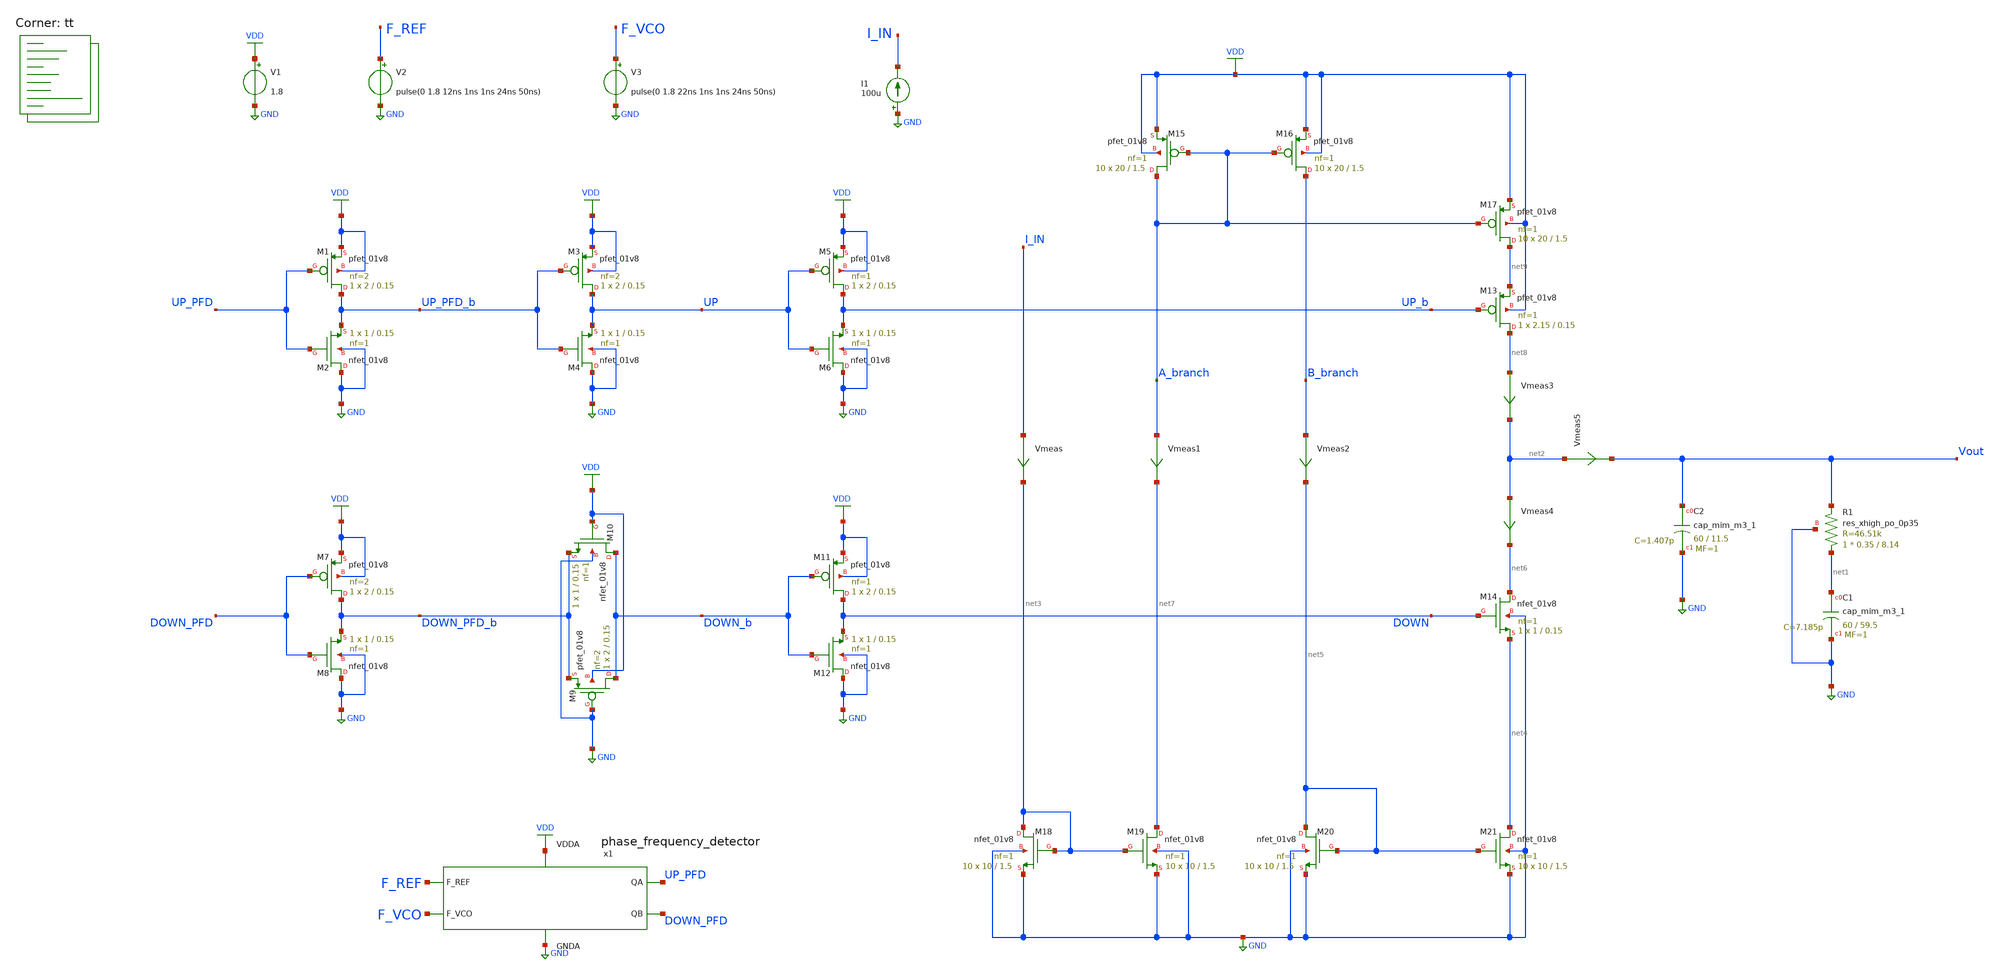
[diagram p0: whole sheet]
** sch_path: projects/pll/charge_pump/xschem_ngspice/pfd_charge_pump_dead_zone_check_2.sch
**.subckt pfd_charge_pump_dead_zone_check_2
V1 VDD GND 1.8
XC2 Vout GND sky130_fd_pr__cap_mim_m3_1 W=60 L=11.5 MF=1 m=1
XC1 net1 GND sky130_fd_pr__cap_mim_m3_1 W=60 L=59.5 MF=1 m=1
V2 F_REF GND pulse(0 1.8 12ns 1ns 1ns 24ns 50ns)
V3 F_VCO GND pulse(0 1.8 22ns 1ns 1ns 24ns 50ns)
x1 F_REF F_VCO VDD UP_PFD DOWN_PFD GND phase_frequency_detector
XR1 net1 Vout GND sky130_fd_pr__res_xhigh_po_0p35 L=8.14 mult=1 m=1
I1 GND I_IN 100u
Vmeas5 net2 Vout 0
.save i(vmeas5)
XM18 net3 net3 GND GND sky130_fd_pr__nfet_01v8 L=1.5 W=10 nf=1 ad='int((nf+1)/2) * W/nf * 0.29' as='int((nf+2)/2) * W/nf * 0.29'
+ pd='2*int((nf+1)/2) * (W/nf + 0.29)' ps='2*int((nf+2)/2) * (W/nf + 0.29)' nrd='0.29 / W' nrs='0.29 / W'
+ sa=0 sb=0 sd=0 mult=10 m=10
XM19 net7 net3 GND GND sky130_fd_pr__nfet_01v8 L=1.5 W=10 nf=1 ad='int((nf+1)/2) * W/nf * 0.29' as='int((nf+2)/2) * W/nf * 0.29'
+ pd='2*int((nf+1)/2) * (W/nf + 0.29)' ps='2*int((nf+2)/2) * (W/nf + 0.29)' nrd='0.29 / W' nrs='0.29 / W'
+ sa=0 sb=0 sd=0 mult=10 m=10
Vmeas I_IN net3 0
.save i(vmeas)
XM13 net8 UP_b net9 VDD sky130_fd_pr__pfet_01v8 L=0.15 W=2.15 nf=1 ad='int((nf+1)/2) * W/nf * 0.29' as='int((nf+2)/2) * W/nf * 0.29'
+ pd='2*int((nf+1)/2) * (W/nf + 0.29)' ps='2*int((nf+2)/2) * (W/nf + 0.29)' nrd='0.29 / W' nrs='0.29 / W'
+ sa=0 sb=0 sd=0 mult=1 m=1
Vmeas3 net8 net2 0
.save i(vmeas3)
Vmeas4 net2 net6 0
.save i(vmeas4)
XM14 net6 DOWN net4 GND sky130_fd_pr__nfet_01v8 L=0.15 W=1 nf=1 ad='int((nf+1)/2) * W/nf * 0.29' as='int((nf+2)/2) * W/nf * 0.29'
+ pd='2*int((nf+1)/2) * (W/nf + 0.29)' ps='2*int((nf+2)/2) * (W/nf + 0.29)' nrd='0.29 / W' nrs='0.29 / W'
+ sa=0 sb=0 sd=0 mult=1 m=1
XM17 net9 A_branch VDD VDD sky130_fd_pr__pfet_01v8 L=1.5 W=20 nf=1 ad='int((nf+1)/2) * W/nf * 0.29' as='int((nf+2)/2) * W/nf * 0.29'
+ pd='2*int((nf+1)/2) * (W/nf + 0.29)' ps='2*int((nf+2)/2) * (W/nf + 0.29)' nrd='0.29 / W' nrs='0.29 / W'
+ sa=0 sb=0 sd=0 mult=10 m=10
XM21 net4 net5 GND GND sky130_fd_pr__nfet_01v8 L=1.5 W=10 nf=1 ad='int((nf+1)/2) * W/nf * 0.29' as='int((nf+2)/2) * W/nf * 0.29'
+ pd='2*int((nf+1)/2) * (W/nf + 0.29)' ps='2*int((nf+2)/2) * (W/nf + 0.29)' nrd='0.29 / W' nrs='0.29 / W'
+ sa=0 sb=0 sd=0 mult=10 m=10
XM20 net5 net5 GND GND sky130_fd_pr__nfet_01v8 L=1.5 W=10 nf=1 ad='int((nf+1)/2) * W/nf * 0.29' as='int((nf+2)/2) * W/nf * 0.29'
+ pd='2*int((nf+1)/2) * (W/nf + 0.29)' ps='2*int((nf+2)/2) * (W/nf + 0.29)' nrd='0.29 / W' nrs='0.29 / W'
+ sa=0 sb=0 sd=0 mult=10 m=10
XM15 A_branch A_branch VDD VDD sky130_fd_pr__pfet_01v8 L=1.5 W=20 nf=1 ad='int((nf+1)/2) * W/nf * 0.29'
+ as='int((nf+2)/2) * W/nf * 0.29' pd='2*int((nf+1)/2) * (W/nf + 0.29)' ps='2*int((nf+2)/2) * (W/nf + 0.29)'
+ nrd='0.29 / W' nrs='0.29 / W' sa=0 sb=0 sd=0 mult=10 m=10
XM16 B_branch A_branch VDD VDD sky130_fd_pr__pfet_01v8 L=1.5 W=20 nf=1 ad='int((nf+1)/2) * W/nf * 0.29'
+ as='int((nf+2)/2) * W/nf * 0.29' pd='2*int((nf+1)/2) * (W/nf + 0.29)' ps='2*int((nf+2)/2) * (W/nf + 0.29)'
+ nrd='0.29 / W' nrs='0.29 / W' sa=0 sb=0 sd=0 mult=10 m=10
Vmeas1 A_branch net7 0
.save i(vmeas1)
Vmeas2 B_branch net5 0
.save i(vmeas2)
XM9 DOWN_b GND DOWN_PFD_b VDD sky130_fd_pr__pfet_01v8 L=0.15 W=2 nf=2 ad='int((nf+1)/2) * W/nf * 0.29'
+ as='int((nf+2)/2) * W/nf * 0.29' pd='2*int((nf+1)/2) * (W/nf + 0.29)' ps='2*int((nf+2)/2) * (W/nf + 0.29)'
+ nrd='0.29 / W' nrs='0.29 / W' sa=0 sb=0 sd=0 mult=1 m=1
XM10 DOWN_b VDD DOWN_PFD_b GND sky130_fd_pr__nfet_01v8 L=0.15 W=1 nf=1 ad='int((nf+1)/2) * W/nf * 0.29'
+ as='int((nf+2)/2) * W/nf * 0.29' pd='2*int((nf+1)/2) * (W/nf + 0.29)' ps='2*int((nf+2)/2) * (W/nf + 0.29)'
+ nrd='0.29 / W' nrs='0.29 / W' sa=0 sb=0 sd=0 mult=1 m=1
XM1 UP_PFD_b UP_PFD VDD VDD sky130_fd_pr__pfet_01v8 L=0.15 W=2 nf=2 ad='int((nf+1)/2) * W/nf * 0.29'
+ as='int((nf+2)/2) * W/nf * 0.29' pd='2*int((nf+1)/2) * (W/nf + 0.29)' ps='2*int((nf+2)/2) * (W/nf + 0.29)'
+ nrd='0.29 / W' nrs='0.29 / W' sa=0 sb=0 sd=0 mult=1 m=1
XM2 GND UP_PFD UP_PFD_b GND sky130_fd_pr__nfet_01v8 L=0.15 W=1 nf=1 ad='int((nf+1)/2) * W/nf * 0.29'
+ as='int((nf+2)/2) * W/nf * 0.29' pd='2*int((nf+1)/2) * (W/nf + 0.29)' ps='2*int((nf+2)/2) * (W/nf + 0.29)'
+ nrd='0.29 / W' nrs='0.29 / W' sa=0 sb=0 sd=0 mult=1 m=1
XM7 DOWN_PFD_b DOWN_PFD VDD VDD sky130_fd_pr__pfet_01v8 L=0.15 W=2 nf=2 ad='int((nf+1)/2) * W/nf * 0.29'
+ as='int((nf+2)/2) * W/nf * 0.29' pd='2*int((nf+1)/2) * (W/nf + 0.29)' ps='2*int((nf+2)/2) * (W/nf + 0.29)'
+ nrd='0.29 / W' nrs='0.29 / W' sa=0 sb=0 sd=0 mult=1 m=1
XM8 GND DOWN_PFD DOWN_PFD_b GND sky130_fd_pr__nfet_01v8 L=0.15 W=1 nf=1 ad='int((nf+1)/2) * W/nf * 0.29'
+ as='int((nf+2)/2) * W/nf * 0.29' pd='2*int((nf+1)/2) * (W/nf + 0.29)' ps='2*int((nf+2)/2) * (W/nf + 0.29)'
+ nrd='0.29 / W' nrs='0.29 / W' sa=0 sb=0 sd=0 mult=1 m=1
XM3 UP UP_PFD_b VDD VDD sky130_fd_pr__pfet_01v8 L=0.15 W=2 nf=2 ad='int((nf+1)/2) * W/nf * 0.29' as='int((nf+2)/2) * W/nf * 0.29'
+ pd='2*int((nf+1)/2) * (W/nf + 0.29)' ps='2*int((nf+2)/2) * (W/nf + 0.29)' nrd='0.29 / W' nrs='0.29 / W'
+ sa=0 sb=0 sd=0 mult=1 m=1
XM4 GND UP_PFD_b UP GND sky130_fd_pr__nfet_01v8 L=0.15 W=1 nf=1 ad='int((nf+1)/2) * W/nf * 0.29' as='int((nf+2)/2) * W/nf * 0.29'
+ pd='2*int((nf+1)/2) * (W/nf + 0.29)' ps='2*int((nf+2)/2) * (W/nf + 0.29)' nrd='0.29 / W' nrs='0.29 / W'
+ sa=0 sb=0 sd=0 mult=1 m=1
XM5 UP_b UP VDD VDD sky130_fd_pr__pfet_01v8 L=0.15 W=2 nf=1 ad='int((nf+1)/2) * W/nf * 0.29' as='int((nf+2)/2) * W/nf * 0.29'
+ pd='2*int((nf+1)/2) * (W/nf + 0.29)' ps='2*int((nf+2)/2) * (W/nf + 0.29)' nrd='0.29 / W' nrs='0.29 / W'
+ sa=0 sb=0 sd=0 mult=1 m=1
XM6 GND UP UP_b GND sky130_fd_pr__nfet_01v8 L=0.15 W=1 nf=1 ad='int((nf+1)/2) * W/nf * 0.29' as='int((nf+2)/2) * W/nf * 0.29'
+ pd='2*int((nf+1)/2) * (W/nf + 0.29)' ps='2*int((nf+2)/2) * (W/nf + 0.29)' nrd='0.29 / W' nrs='0.29 / W'
+ sa=0 sb=0 sd=0 mult=1 m=1
XM11 DOWN DOWN_b VDD VDD sky130_fd_pr__pfet_01v8 L=0.15 W=2 nf=1 ad='int((nf+1)/2) * W/nf * 0.29' as='int((nf+2)/2) * W/nf * 0.29'
+ pd='2*int((nf+1)/2) * (W/nf + 0.29)' ps='2*int((nf+2)/2) * (W/nf + 0.29)' nrd='0.29 / W' nrs='0.29 / W'
+ sa=0 sb=0 sd=0 mult=1 m=1
XM12 GND DOWN_b DOWN GND sky130_fd_pr__nfet_01v8 L=0.15 W=1 nf=1 ad='int((nf+1)/2) * W/nf * 0.29' as='int((nf+2)/2) * W/nf * 0.29'
+ pd='2*int((nf+1)/2) * (W/nf + 0.29)' ps='2*int((nf+2)/2) * (W/nf + 0.29)' nrd='0.29 / W' nrs='0.29 / W'
+ sa=0 sb=0 sd=0 mult=1 m=1
**** begin user architecture code
.lib $::SKYWATER_MODELS/sky130.lib.spice tt



**** end user architecture code
**.ends

* expanding   symbol:
*+  /foss/designs/my_design/projects/pll/pfd/xschem_ngspice/phase_frequency_detector.sym # of pins=6
** sym_path: projects/pll/pfd/xschem_ngspice/phase_frequency_detector.sym
** sch_path: projects/pll/pfd/xschem_ngspice/phase_frequency_detector.sch
.subckt phase_frequency_detector F_REF F_VCO VDDA QA QB GNDA
*.ipin F_REF
*.opin QA
*.ipin F_VCO
*.opin QB
*.ipin VDDA
*.ipin GNDA
x1 F_REF QA GNDA GNDA VDDA VDDA QA_b sky130_fd_sc_hd__nor2_1
x2 QA_b E GNDA GNDA VDDA VDDA QA sky130_fd_sc_hd__nor2_1
x3 QA_b E_b GNDA GNDA VDDA VDDA E sky130_fd_sc_hd__nor2_1
x4 E Reset GNDA GNDA VDDA VDDA E_b sky130_fd_sc_hd__nor2_1
x5 F_VCO QB GNDA GNDA VDDA VDDA QB_b sky130_fd_sc_hd__nor2_1
x6 QB_b F GNDA GNDA VDDA VDDA QB sky130_fd_sc_hd__nor2_1
x7 QB_b F_b GNDA GNDA VDDA VDDA F sky130_fd_sc_hd__nor2_1
x8 F Reset GNDA GNDA VDDA VDDA F_b sky130_fd_sc_hd__nor2_1
x9 QA QB GNDA GNDA VDDA VDDA before_Reset sky130_fd_sc_hd__nand2_1
x10 before_Reset GNDA GNDA VDDA VDDA net1 sky130_fd_sc_hd__inv_1
x11 net1 GNDA GNDA VDDA VDDA net2 sky130_fd_sc_hd__inv_1
x12 net2 GNDA GNDA VDDA VDDA net3 sky130_fd_sc_hd__inv_1
x13 net3 GNDA GNDA VDDA VDDA net4 sky130_fd_sc_hd__inv_1
x14 net4 GNDA GNDA VDDA VDDA Reset sky130_fd_sc_hd__inv_1
.ends

.GLOBAL GND
.GLOBAL VDD
.end
